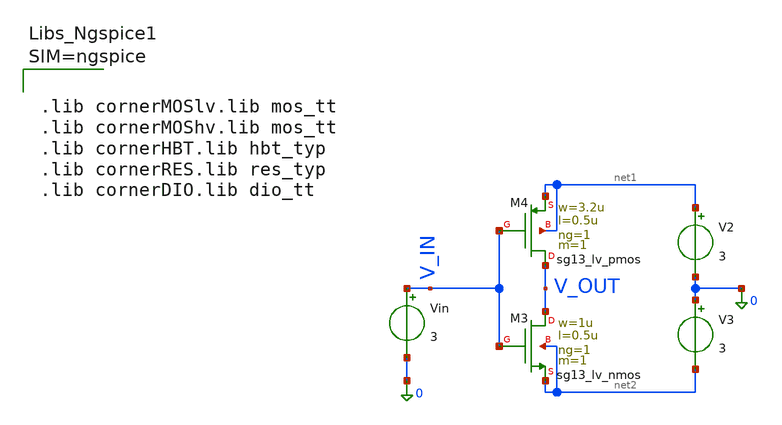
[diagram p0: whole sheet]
** sch_path: 000_Xschemplayground/Inverter/Inverter Daniel.sch
**.subckt Inverter Daniel
V2 net1 0 3
V3 0 net2 3
XM3 V_OUT V_IN net2 net2 sg13_lv_nmos w=1u l=0.5u ng=1 m=1 mm_ok=1
XM4 V_OUT V_IN net1 net1 sg13_lv_pmos w=3.2u l=0.5u ng=1 m=1 mm_ok=1
Vin V_IN 0 3
**** begin user architecture code


.dc vin -1.5 1.5 0.1
.save all
.control
run
plot v(V_OUT) vs v(V_IN)
.endc





.lib cornerMOSlv.lib mos_tt
.lib cornerMOShv.lib mos_tt
.lib cornerHBT.lib hbt_typ
.lib cornerRES.lib res_typ
.lib cornerDIO.lib dio_tt



**** end user architecture code
**.ends
.end
